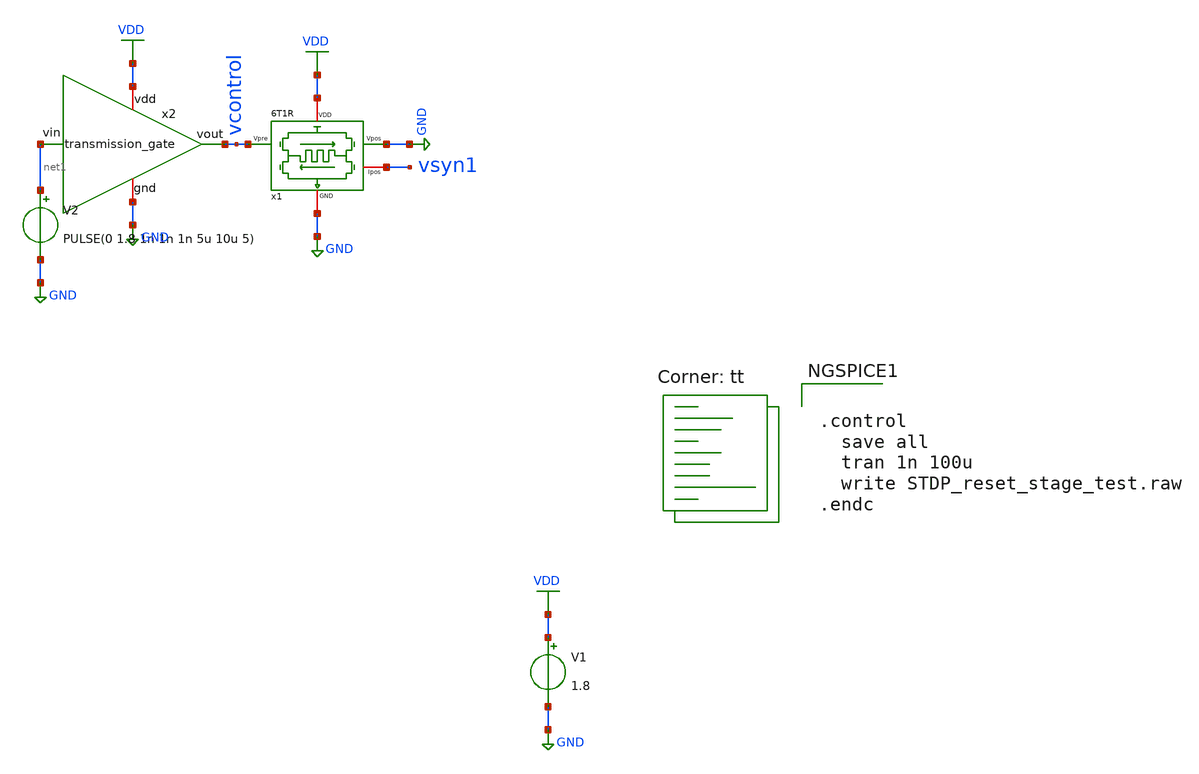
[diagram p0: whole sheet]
** sch_path: STDP/STDP_reset_stage_test.sch
**.subckt STDP_reset_stage_test
V1 VDD GND 1.8
x1 VDD vsyn1 vcontrol GND GND 6T1R
V2 net1 GND PULSE(0 1.8 1n 1n 1n 5u 10u 5)
x2 net1 GND VDD vcontrol transmission_gate
**** begin user architecture code
.lib $::SKYWATER_MODELS/sky130.lib.spice tt

** opencircuitdesign pdks install
.inc $::SKYWATER_MODELS/rram_v0.spice



.control
  save all
  tran 1n 100u
  write STDP_reset_stage_test.raw
.endc


**** end user architecture code
**.ends
.GLOBAL GND
.GLOBAL VDD
.end
